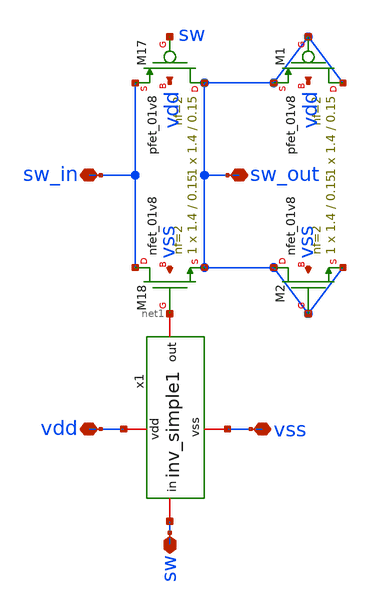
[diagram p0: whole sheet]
** sch_path: xschem/tgate_1.sch
**.subckt tgate_1 sw_in vdd vss sw sw_out
*.iopin sw_in
*.iopin vdd
*.iopin vss
*.iopin sw
*.iopin sw_out
XM17 sw_out sw sw_in vdd sky130_fd_pr__pfet_01v8 L=0.15 W=1.4 nf=2 ad='int((nf+1)/2) * W/nf * 0.29' as='int((nf+2)/2) * W/nf * 0.29'
+ pd='2*int((nf+1)/2) * (W/nf + 0.29)' ps='2*int((nf+2)/2) * (W/nf + 0.29)' nrd='0.29 / W' nrs='0.29 / W'
+ sa=0 sb=0 sd=0 mult=1 m=1
XM18 sw_in net1 sw_out vss sky130_fd_pr__nfet_01v8 L=0.15 W=1.4 nf=2 ad='int((nf+1)/2) * W/nf * 0.29'
+ as='int((nf+2)/2) * W/nf * 0.29' pd='2*int((nf+1)/2) * (W/nf + 0.29)' ps='2*int((nf+2)/2) * (W/nf + 0.29)'
+ nrd='0.29 / W' nrs='0.29 / W' sa=0 sb=0 sd=0 mult=1 m=1
x1 vdd sw net1 vss inv_simple1
XM1 sw_out sw_out sw_out vdd sky130_fd_pr__pfet_01v8 L=0.15 W=1.4 nf=2 ad='int((nf+1)/2) * W/nf * 0.29'
+ as='int((nf+2)/2) * W/nf * 0.29' pd='2*int((nf+1)/2) * (W/nf + 0.29)' ps='2*int((nf+2)/2) * (W/nf + 0.29)'
+ nrd='0.29 / W' nrs='0.29 / W' sa=0 sb=0 sd=0 mult=1 m=1
XM2 sw_out sw_out sw_out vss sky130_fd_pr__nfet_01v8 L=0.15 W=1.4 nf=2 ad='int((nf+1)/2) * W/nf * 0.29'
+ as='int((nf+2)/2) * W/nf * 0.29' pd='2*int((nf+1)/2) * (W/nf + 0.29)' ps='2*int((nf+2)/2) * (W/nf + 0.29)'
+ nrd='0.29 / W' nrs='0.29 / W' sa=0 sb=0 sd=0 mult=1 m=1
**.ends

* expanding   symbol:  inv_simple1.sym # of pins=4
** sym_path: xschem/inv_simple1.sym
** sch_path: xschem/inv_simple1.sch
.subckt inv_simple1 vdd in out vss
*.iopin in
*.iopin vdd
*.iopin vss
*.iopin out
XM19 out in vss vss sky130_fd_pr__nfet_01v8 L=0.15 W=1.4 nf=1 ad='int((nf+1)/2) * W/nf * 0.29' as='int((nf+2)/2) * W/nf * 0.29'
+ pd='2*int((nf+1)/2) * (W/nf + 0.29)' ps='2*int((nf+2)/2) * (W/nf + 0.29)' nrd='0.29 / W' nrs='0.29 / W'
+ sa=0 sb=0 sd=0 mult=1 m=1
XM20 out in vdd vdd sky130_fd_pr__pfet_01v8 L=0.15 W=2.8 nf=1 ad='int((nf+1)/2) * W/nf * 0.29' as='int((nf+2)/2) * W/nf * 0.29'
+ pd='2*int((nf+1)/2) * (W/nf + 0.29)' ps='2*int((nf+2)/2) * (W/nf + 0.29)' nrd='0.29 / W' nrs='0.29 / W'
+ sa=0 sb=0 sd=0 mult=1 m=1
XM1 vdd vdd vdd vdd sky130_fd_pr__pfet_01v8 L=0.15 W=1.4 nf=1 ad='int((nf+1)/2) * W/nf * 0.29' as='int((nf+2)/2) * W/nf * 0.29'
+ pd='2*int((nf+1)/2) * (W/nf + 0.29)' ps='2*int((nf+2)/2) * (W/nf + 0.29)' nrd='0.29 / W' nrs='0.29 / W'
+ sa=0 sb=0 sd=0 mult=1 m=1
XM2 vss vss vss vss sky130_fd_pr__nfet_01v8 L=0.15 W=1.4 nf=1 ad='int((nf+1)/2) * W/nf * 0.29' as='int((nf+2)/2) * W/nf * 0.29'
+ pd='2*int((nf+1)/2) * (W/nf + 0.29)' ps='2*int((nf+2)/2) * (W/nf + 0.29)' nrd='0.29 / W' nrs='0.29 / W'
+ sa=0 sb=0 sd=0 mult=1 m=1
.ends

.end
